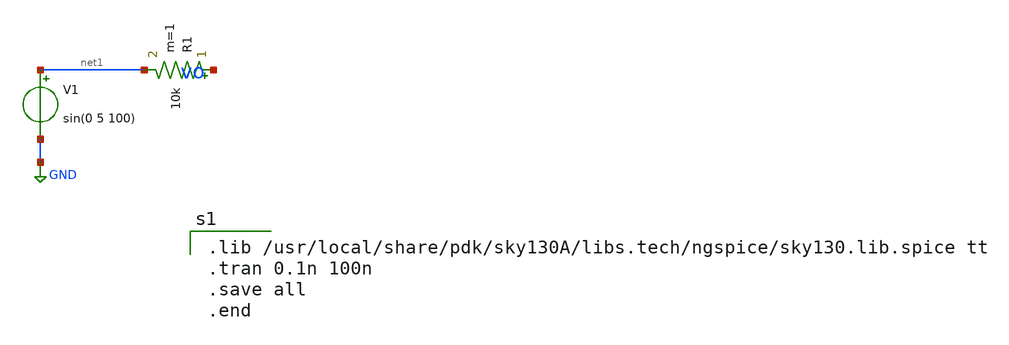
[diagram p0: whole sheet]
** sch_path: documents/noise.sch
**.subckt noise
R1 vo net1 10k m=1
V1 net1 GND sin(0 5 100)
**** begin user architecture code

.lib /usr/local/share/pdk/sky130A/libs.tech/ngspice/sky130.lib.spice tt
.tran 0.1n 100n
.save all
.end

**** end user architecture code
**.ends
.GLOBAL GND
.end
